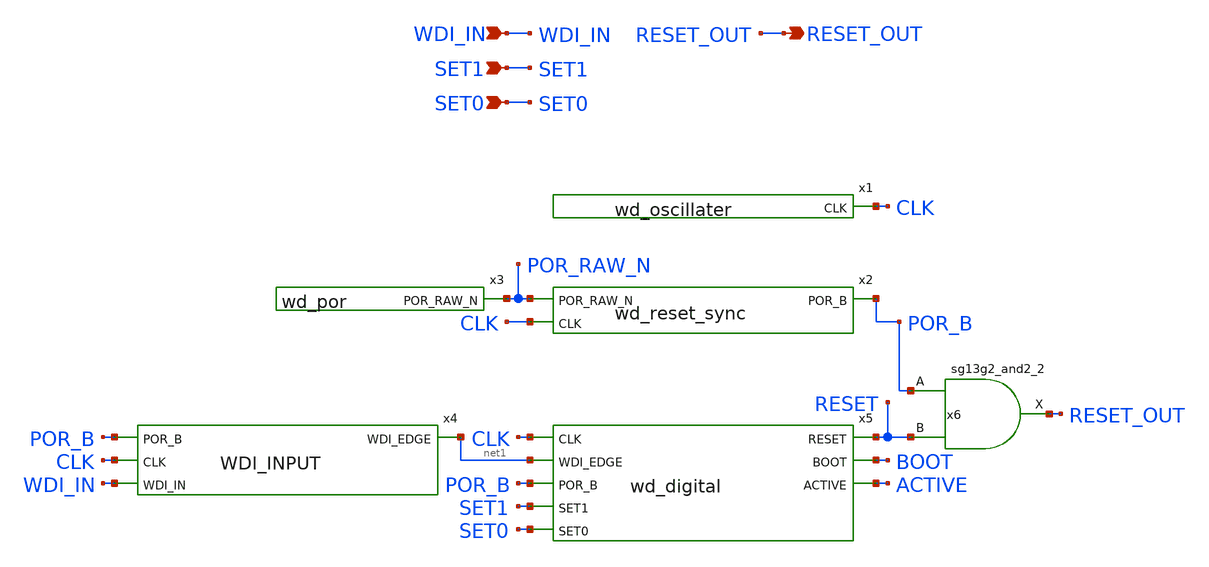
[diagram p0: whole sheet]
** sch_path: design/top/schematic/wd_watchdog.sch
**.subckt wd_watchdog SET1 SET0 WDI_IN RESET_OUT
*.ipin SET1
*.ipin SET0
*.ipin WDI_IN
*.opin RESET_OUT
x1 CLK VDD VSS wd_oscillater
x2 POR_RAW_N CLK POR_B VDD VSS wd_reset_sync
x3 POR_RAW_N VDD VSS wd_por
x4 POR_B CLK WDI_IN net1 WDI_INPUT
x5 RESET BOOT CLK net1 ACTIVE POR_B SET1 SET0 VDD VSS wd_digital
x6 RESET_OUT POR_B RESET VDD VSS sg13g2_and2_2
**.ends
.end
